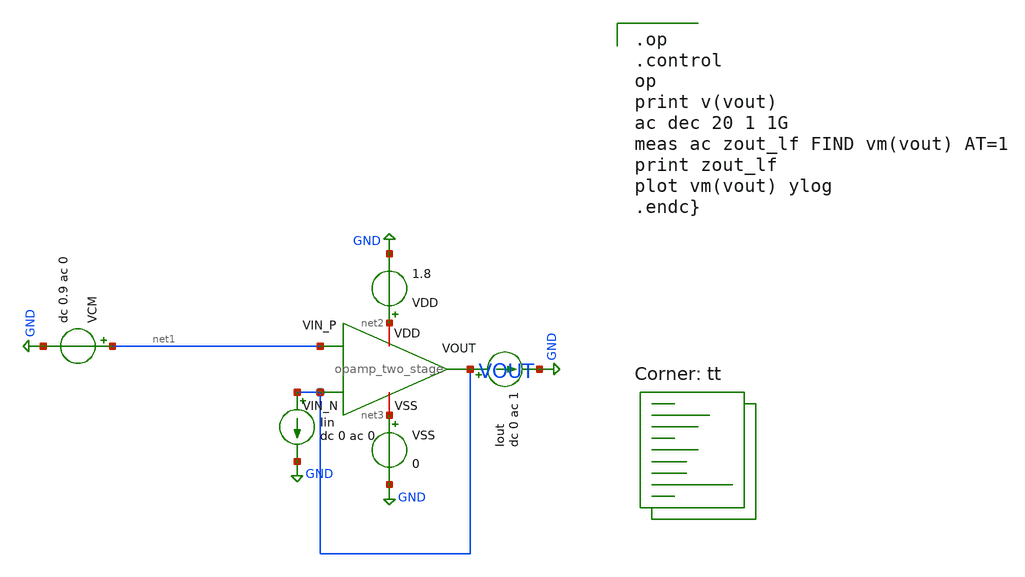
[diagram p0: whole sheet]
** sch_path: analog/bootcamp_opamp/schematics/tb_impedance.sch
**.subckt tb_impedance
x1 net2 VOUT net1 VOUT net3 opamp_two_stage
VSS net3 GND 0
VDD net2 GND 1.8
VCM net1 GND dc 0.9 ac 0
Iout VOUT GND dc 0 ac 1
Iin VOUT GND dc 0 ac 0
**** begin user architecture code

.op
.control
op
print v(vout)
ac dec 20 1 1G
meas ac zout_lf FIND vm(vout) AT=1
print zout_lf
plot vm(vout) ylog
.endc}

.lib $::SKYWATER_MODELS/sky130.lib.spice tt
**** end user architecture code
**.ends
.GLOBAL GND
.end
